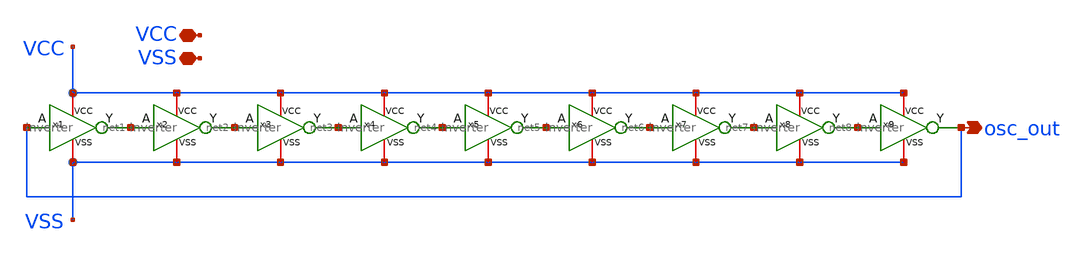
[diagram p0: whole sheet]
** sch_path: xschem/basicring9.sch
**.subckt basicring9 osc_out VCC VSS
*.opin osc_out
*.iopin VCC
*.iopin VSS
x1 VCC VSS net1 osc_out inverter
x2 VCC VSS net2 net1 inverter
x3 VCC VSS net3 net2 inverter
x4 VCC VSS net4 net3 inverter
x5 VCC VSS net5 net4 inverter
x6 VCC VSS net6 net5 inverter
x7 VCC VSS net7 net6 inverter
x8 VCC VSS net8 net7 inverter
x9 VCC VSS osc_out net8 inverter
**.ends

* expanding   symbol:  inverter.sym # of pins=4
** sym_path: xschem/inverter.sym
** sch_path: xschem/inverter.sch
.subckt inverter VCC VSS Y A
*.iopin VCC
*.iopin VSS
*.ipin A
*.opin Y
XM1 Y A VSS VSS nfet_03v3 L=0.50u W=0.25u nf=1 ad='int((nf+1)/2) * W/nf * 0.18u' as='int((nf+2)/2) * W/nf * 0.18u'
+ pd='2*int((nf+1)/2) * (W/nf + 0.18u)' ps='2*int((nf+2)/2) * (W/nf + 0.18u)' nrd='0.18u / W' nrs='0.18u / W'
+ sa=0 sb=0 sd=0 m=1
XM2 Y A VCC VCC pfet_03v3 L=0.50u W=0.50u nf=1 ad='int((nf+1)/2) * W/nf * 0.18u' as='int((nf+2)/2) * W/nf * 0.18u'
+ pd='2*int((nf+1)/2) * (W/nf + 0.18u)' ps='2*int((nf+2)/2) * (W/nf + 0.18u)' nrd='0.18u / W' nrs='0.18u / W'
+ sa=0 sb=0 sd=0 m=1
.ends

.end
